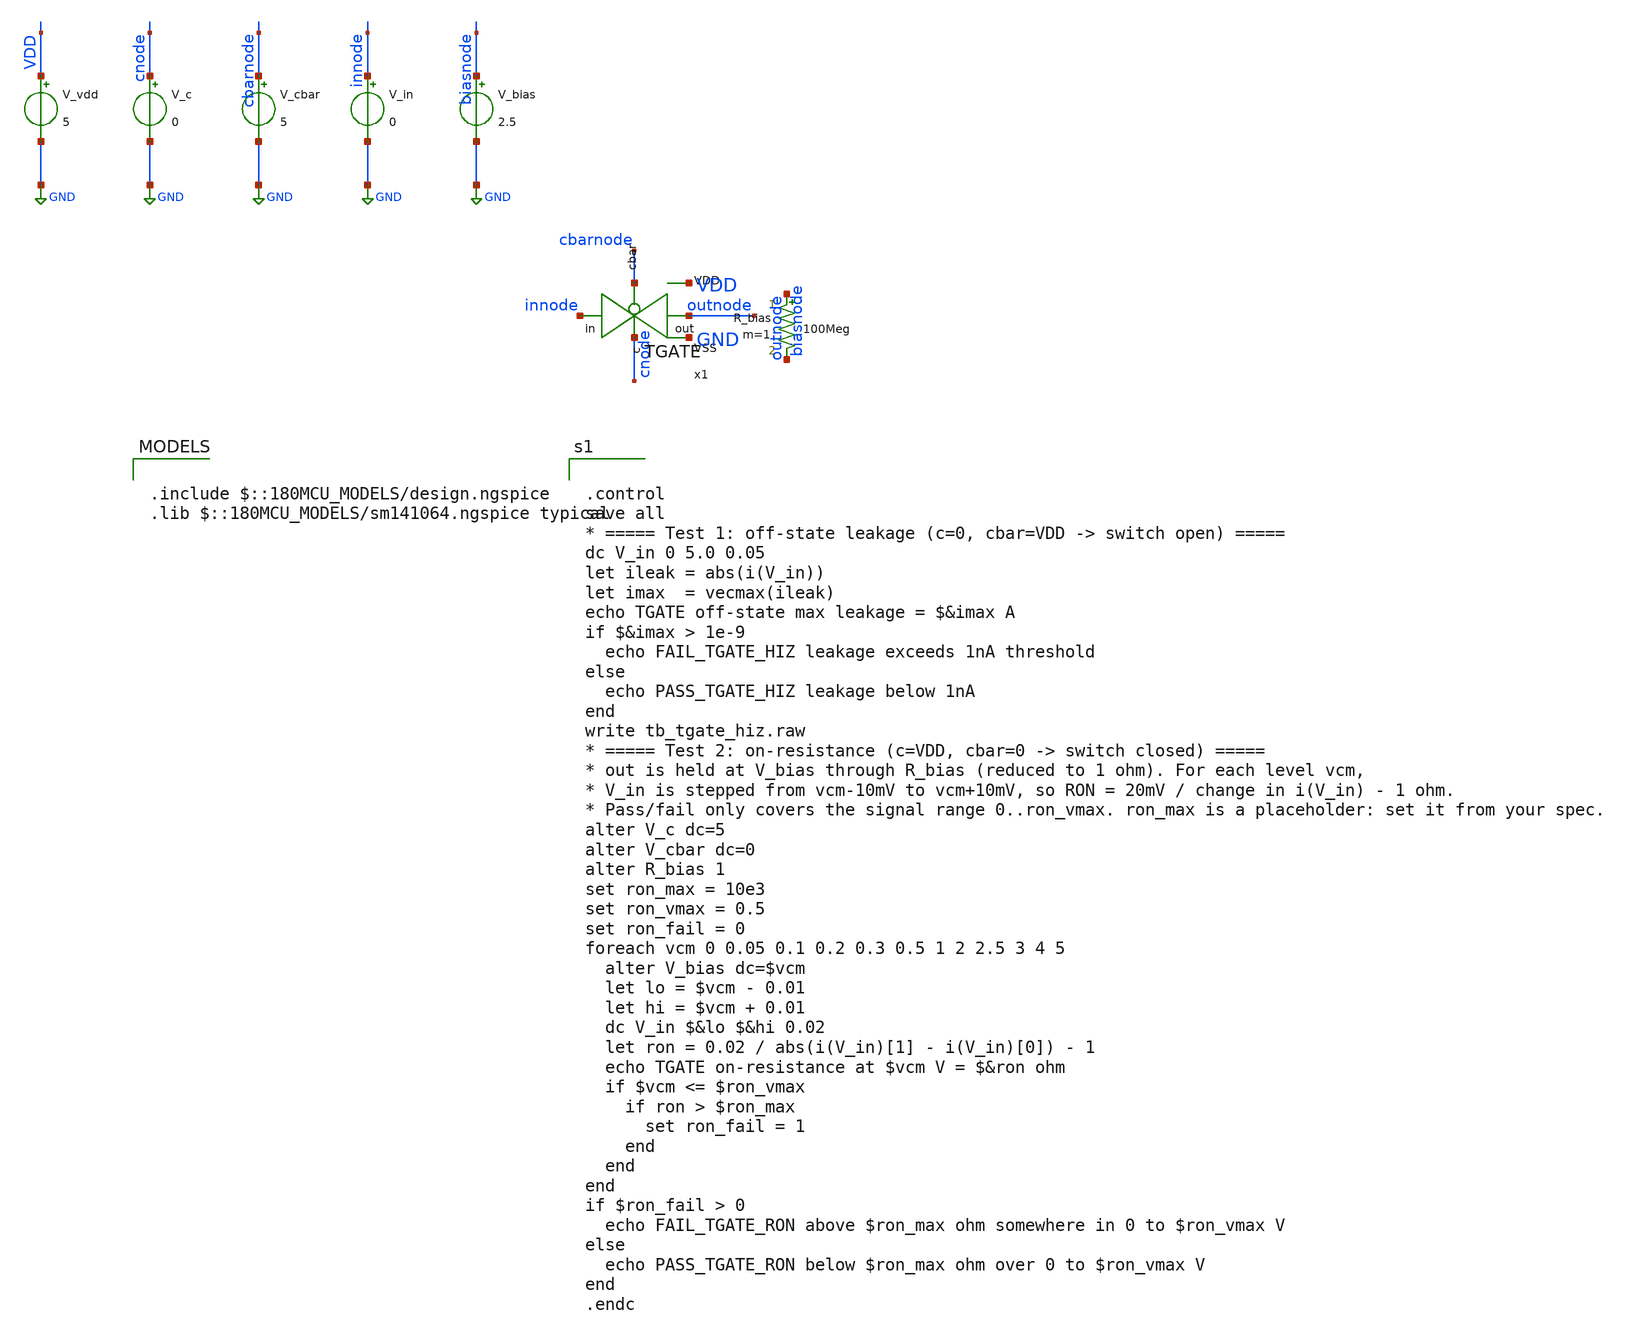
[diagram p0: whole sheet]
** sch_path: TGATE/tb_tgate_hiz.sch
**.subckt tb_tgate_hiz
V_vdd VDD GND 5
V_c cnode GND 0
V_cbar cbarnode GND 5
V_in innode GND 0
.save i(v_in)
V_bias biasnode GND 2.5
R_bias outnode biasnode 100Meg m=1
x1 outnode cnode cbarnode innode VDD GND TGATE
**** begin user architecture code

.include $::180MCU_MODELS/design.ngspice
.lib $::180MCU_MODELS/sm141064.ngspice typical



.control
save all
* ===== Test 1: off-state leakage (c=0, cbar=VDD -> switch open) =====
dc V_in 0 5.0 0.05
let ileak = abs(i(V_in))
let imax  = vecmax(ileak)
echo TGATE off-state max leakage = $&imax A
if $&imax > 1e-9
  echo FAIL_TGATE_HIZ leakage exceeds 1nA threshold
else
  echo PASS_TGATE_HIZ leakage below 1nA
end
write tb_tgate_hiz.raw
* ===== Test 2: on-resistance (c=VDD, cbar=0 -> switch closed) =====
* out is held at V_bias through R_bias (reduced to 1 ohm). For each level vcm,
* V_in is stepped from vcm-10mV to vcm+10mV, so RON = 20mV / change in i(V_in) - 1 ohm.
* Pass/fail only covers the signal range 0..ron_vmax. ron_max is a placeholder: set it from your
*+ spec.
alter V_c dc=5
alter V_cbar dc=0
alter R_bias 1
set ron_max = 10e3
set ron_vmax = 0.5
set ron_fail = 0
foreach vcm 0 0.05 0.1 0.2 0.3 0.5 1 2 2.5 3 4 5
  alter V_bias dc=$vcm
  let lo = $vcm - 0.01
  let hi = $vcm + 0.01
  dc V_in $&lo $&hi 0.02
  let ron = 0.02 / abs(i(V_in)[1] - i(V_in)[0]) - 1
  echo TGATE on-resistance at $vcm V = $&ron ohm
  if $vcm <= $ron_vmax
    if ron > $ron_max
      set ron_fail = 1
    end
  end
end
if $ron_fail > 0
  echo FAIL_TGATE_RON above $ron_max ohm somewhere in 0 to $ron_vmax V
else
  echo PASS_TGATE_RON below $ron_max ohm over 0 to $ron_vmax V
end
.endc


**** end user architecture code
**.ends

* expanding   symbol:  TGATE.sym # of pins=6
** sym_path: TGATE/TGATE.sym
** sch_path: TGATE/TGATE.sch
.subckt TGATE out c cbar in VDD VSS
*.ipin in
*.opin out
*.ipin cbar
*.ipin c
*.iopin VDD
*.iopin VSS
XM1 out cbar in VDD pfet_05v0 L=0.6u W=1.22u nf=1 ad='int((nf+1)/2) * W/nf * 0.18u' as='int((nf+2)/2) * W/nf * 0.18u'
+ pd='2*int((nf+1)/2) * (W/nf + 0.18u)' ps='2*int((nf+2)/2) * (W/nf + 0.18u)' nrd='0.18u / W' nrs='0.18u / W'
+ sa=0 sb=0 sd=0 m=1
XM2 out c in VSS nfet_05v0 L=0.6u W=0.565u nf=1 ad='int((nf+1)/2) * W/nf * 0.18u' as='int((nf+2)/2) * W/nf * 0.18u'
+ pd='2*int((nf+1)/2) * (W/nf + 0.18u)' ps='2*int((nf+2)/2) * (W/nf + 0.18u)' nrd='0.18u / W' nrs='0.18u / W'
+ sa=0 sb=0 sd=0 m=1
.ends

.GLOBAL GND
.end
